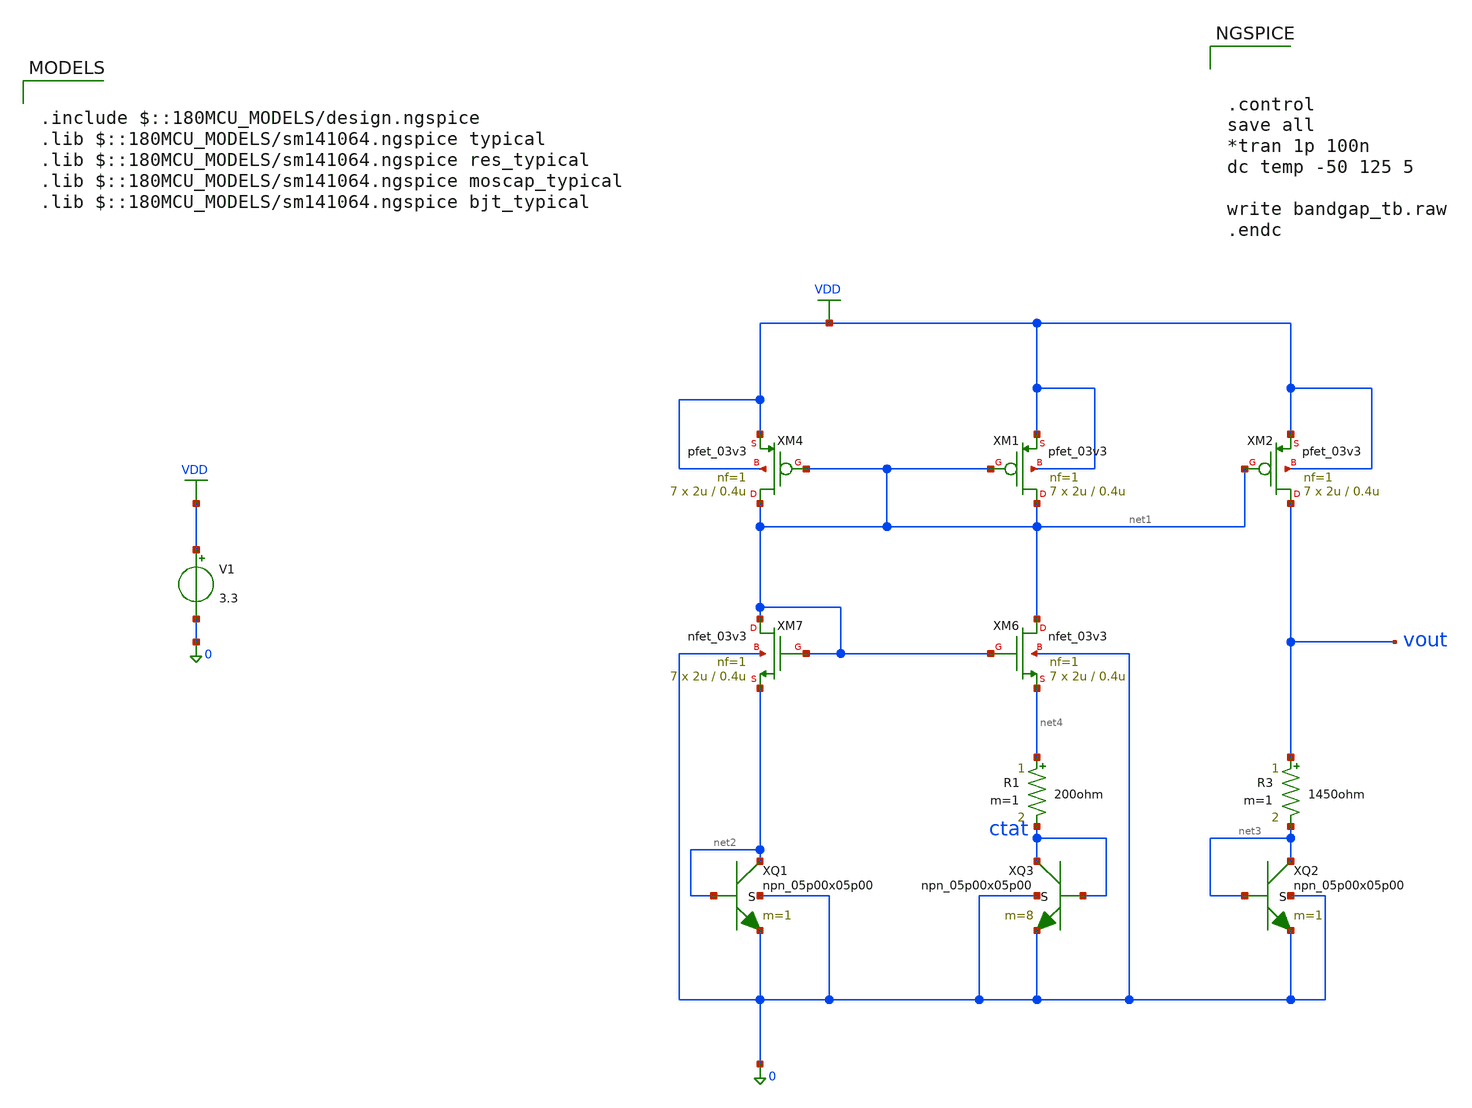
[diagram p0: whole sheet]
** sch_path: BGR_LDO/test_bgr.sch
**.subckt test_bgr
V1 VDD 0 3.3
.save i(v1)
XM1 net1 net1 VDD VDD pfet_03v3 L=0.4u W=2u nf=1 ad='int((nf+1)/2) * W/nf * 0.18u' as='int((nf+2)/2) * W/nf * 0.18u'
+ pd='2*int((nf+1)/2) * (W/nf + 0.18u)' ps='2*int((nf+2)/2) * (W/nf + 0.18u)' nrd='0.18u / W' nrs='0.18u / W'
+ sa=0 sb=0 sd=0 m=7
XM4 net1 net1 VDD VDD pfet_03v3 L=0.4u W=2u nf=1 ad='int((nf+1)/2) * W/nf * 0.18u' as='int((nf+2)/2) * W/nf * 0.18u'
+ pd='2*int((nf+1)/2) * (W/nf + 0.18u)' ps='2*int((nf+2)/2) * (W/nf + 0.18u)' nrd='0.18u / W' nrs='0.18u / W'
+ sa=0 sb=0 sd=0 m=7
XM6 net1 net1 net4 0 nfet_03v3 L=0.4u W=2u nf=1 ad='int((nf+1)/2) * W/nf * 0.18u' as='int((nf+2)/2) * W/nf * 0.18u'
+ pd='2*int((nf+1)/2) * (W/nf + 0.18u)' ps='2*int((nf+2)/2) * (W/nf + 0.18u)' nrd='0.18u / W' nrs='0.18u / W'
+ sa=0 sb=0 sd=0 m=7
XM7 net1 net1 net2 0 nfet_03v3 L=0.4u W=2u nf=1 ad='int((nf+1)/2) * W/nf * 0.18u' as='int((nf+2)/2) * W/nf * 0.18u'
+ pd='2*int((nf+1)/2) * (W/nf + 0.18u)' ps='2*int((nf+2)/2) * (W/nf + 0.18u)' nrd='0.18u / W' nrs='0.18u / W'
+ sa=0 sb=0 sd=0 m=7
R1 net4 ctat 200ohm m=1
XM2 vout net1 VDD VDD pfet_03v3 L=0.4u W=2u nf=1 ad='int((nf+1)/2) * W/nf * 0.18u' as='int((nf+2)/2) * W/nf * 0.18u'
+ pd='2*int((nf+1)/2) * (W/nf + 0.18u)' ps='2*int((nf+2)/2) * (W/nf + 0.18u)' nrd='0.18u / W' nrs='0.18u / W'
+ sa=0 sb=0 sd=0 m=7
R3 vout net3 1450ohm m=1
XQ1 net2 net2 0 0 npn_05p00x05p00 m=1
XQ2 net3 net3 0 0 npn_05p00x05p00 m=1
XQ3 ctat ctat 0 0 npn_05p00x05p00 m=8
**** begin user architecture code

.include $::180MCU_MODELS/design.ngspice
.lib $::180MCU_MODELS/sm141064.ngspice typical
.lib $::180MCU_MODELS/sm141064.ngspice res_typical
.lib $::180MCU_MODELS/sm141064.ngspice moscap_typical
.lib $::180MCU_MODELS/sm141064.ngspice bjt_typical




.control
save all
*tran 1p 100n
dc temp -50 125 5

write bandgap_tb.raw
.endc


**** end user architecture code
**.ends
.GLOBAL VDD
.end
